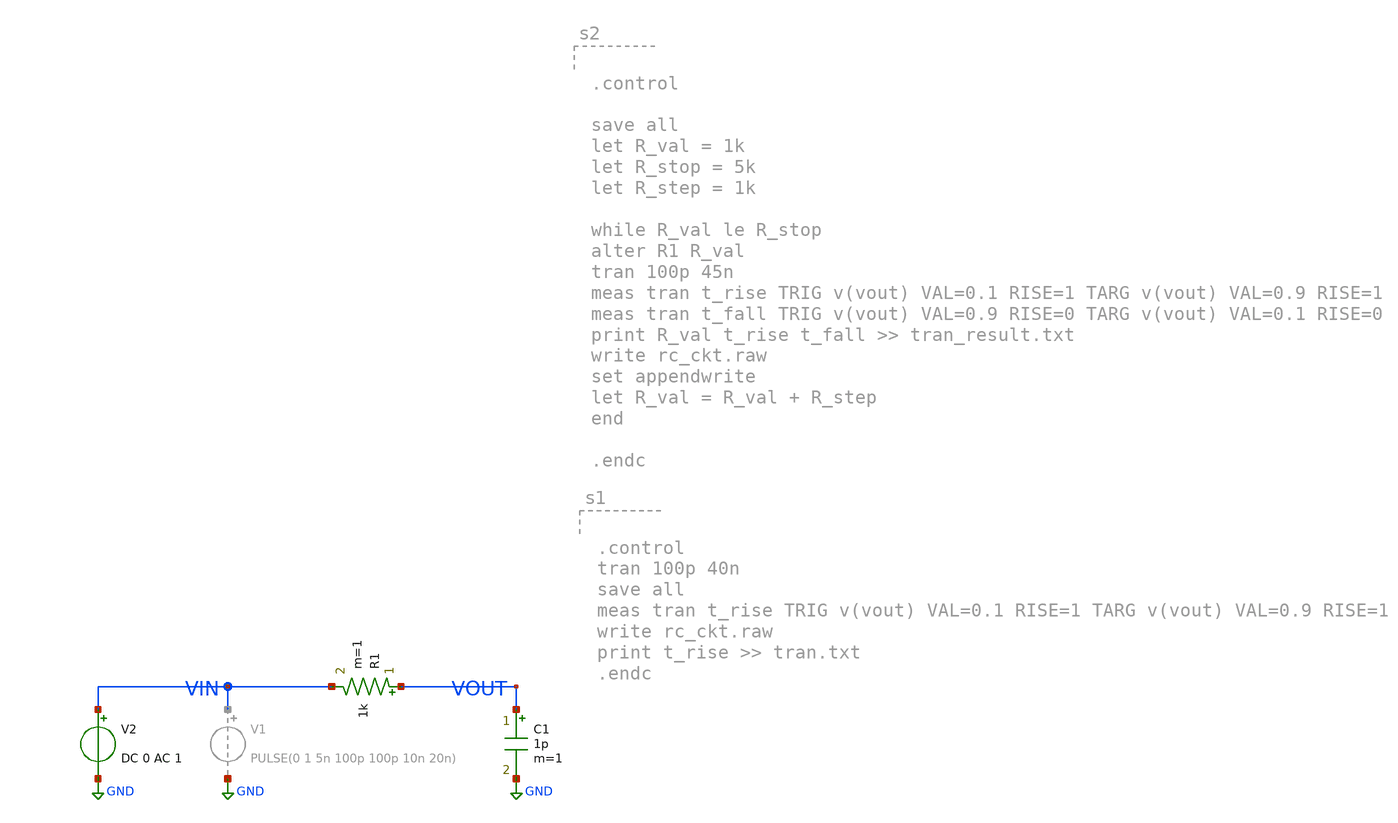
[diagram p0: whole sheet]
** sch_path: ITI_Labs/Lab1/RC/Design/RC.sch
**.subckt RC
C1 VOUT GND 1p m=1
R1 VOUT VIN 1k m=1
V2 VIN GND DC 0 AC 1
**** begin user architecture code


.control

save all

let R_val = 1k
let R_stop = 1meg
let R_mult = 10

while R_val le R_stop
alter R1 R_val
ac dec 10 1 10g

meas ac MAX_GAIN MAX vmag(vout) FROM=1 TO=10G
meas ac BW WHEN vmag(vout)=0.707 FALL=1

print MAX_GAIN BW >> ac_result.txt
write rc_ckt_2.raw
set appendwrite
let R_val = R_val * R_mult
end

.endc


**** end user architecture code
**.ends
.GLOBAL GND
.end
